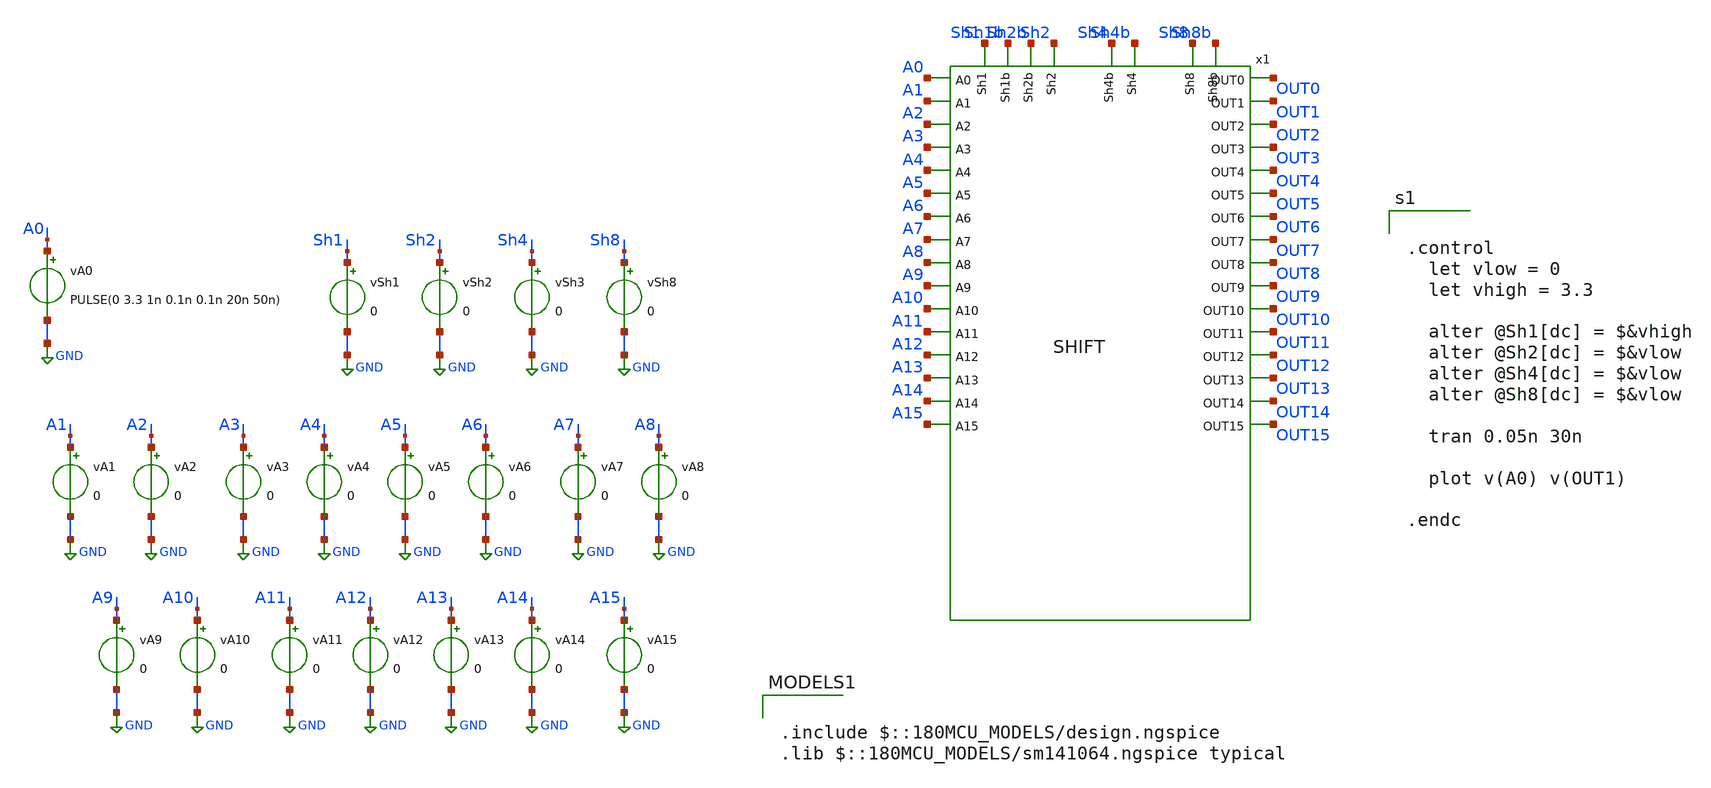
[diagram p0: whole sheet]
** sch_path: shift_rise_tb.sch
**.subckt shift_rise_tb
vA0 A0 GND PULSE(0 3.3 1n 0.1n 0.1n 20n 50n)
vA1 A1 GND 0
vA2 A2 GND 0
vA3 A3 GND 0
vA4 A4 GND 0
vA5 A5 GND 0
vA6 A6 GND 0
vA7 A7 GND 0
vA8 A8 GND 0
vA9 A9 GND 0
vA10 A10 GND 0
vA11 A11 GND 0
vA12 A12 GND 0
vA13 A13 GND 0
vA14 A14 GND 0
vA15 A15 GND 0
vSh1 Sh1 GND 0
vSh2 Sh2 GND 0
vSh3 Sh4 GND 0
vSh8 Sh8 GND 0
x1 Sh1b Sh1 Sh2 Sh2b A0 OUT0 A1 OUT1 Sh4b Sh4 A2 OUT2 A3 OUT3 Sh8b Sh8 OUT4 A4 OUT5 A5 OUT6 A6 OUT7
+ A7 OUT8 A8 A9 OUT9 A10 OUT10 OUT11 A11 OUT12 A12 A13 OUT13 OUT14 A14 OUT15 A15 SHIFT
**** begin user architecture code

.include $::180MCU_MODELS/design.ngspice
.lib $::180MCU_MODELS/sm141064.ngspice typical



.control
  let vlow = 0
  let vhigh = 3.3

  alter @Sh1[dc] = $&vhigh
  alter @Sh2[dc] = $&vlow
  alter @Sh4[dc] = $&vlow
  alter @Sh8[dc] = $&vlow

  tran 0.05n 30n

  plot v(A0) v(OUT1)

.endc


**** end user architecture code
**.ends
.GLOBAL GND
.end
